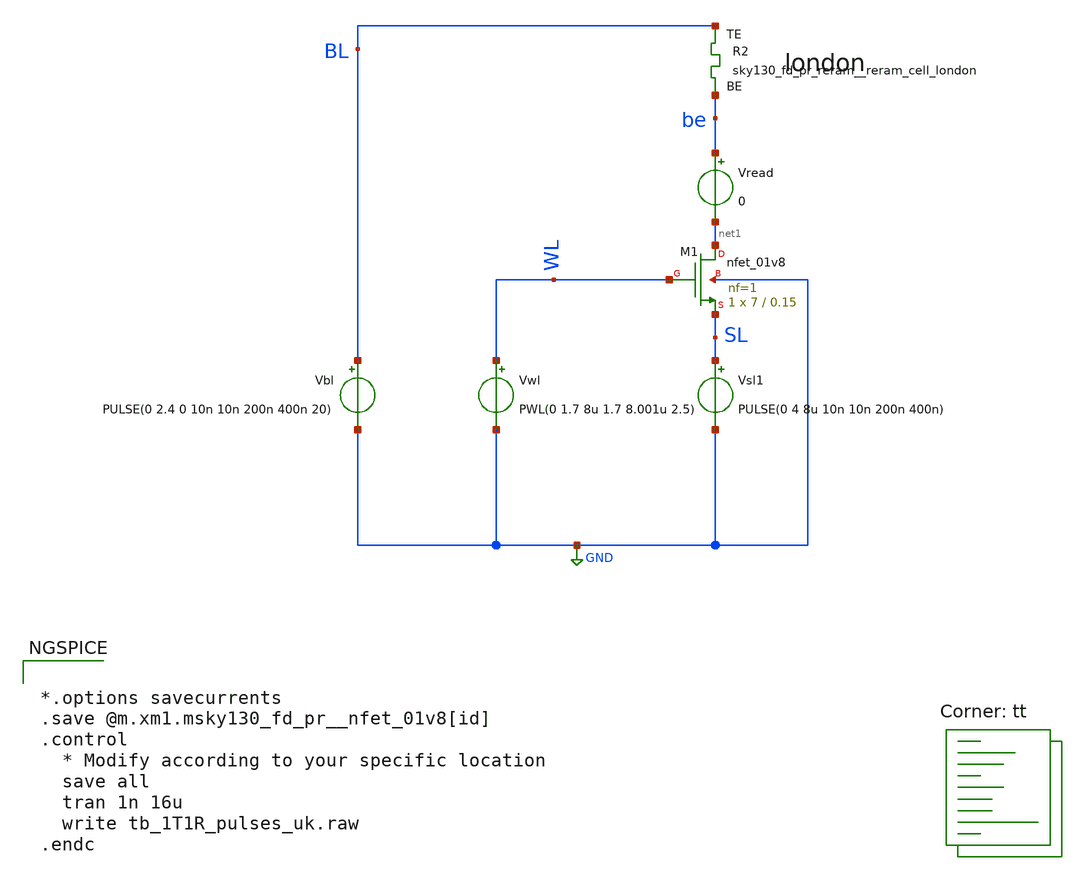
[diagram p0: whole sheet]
** sch_path: memristor_models/rram_london/tb_1T1R_pulses_uk.sch
**.subckt tb_1T1R_pulses_uk
XM1 net1 WL SL GND sky130_fd_pr__nfet_01v8 L=0.15 W=7 nf=1 ad='int((nf+1)/2) * W/nf * 0.29' as='int((nf+2)/2) * W/nf * 0.29'
+ pd='2*int((nf+1)/2) * (W/nf + 0.29)' ps='2*int((nf+2)/2) * (W/nf + 0.29)' nrd='0.29 / W' nrs='0.29 / W'
+ sa=0 sb=0 sd=0 mult=1 m=1
Vwl WL GND PWL(0 1.7 8u 1.7 8.001u 2.5)
Vbl BL GND PULSE(0 2.4 0 10n 10n 200n 400n 20)
XR2 BL be sky130_fd_pr_reram__reram_cell_london
Vread be net1 0
Vsl1 SL GND PULSE(0 4 8u 10n 10n 200n 400n)
**** begin user architecture code


*.options savecurrents
.save @m.xm1.msky130_fd_pr__nfet_01v8[id]
.control
  * Modify according to your specific location
  save all
  tran 1n 16u
  write tb_1T1R_pulses_uk.raw
.endc



.lib $::SKYWATER_MODELS/sky130.lib.spice tt

** opencircuitdesign pdks install
.inc $::SKYWATER_MODELS/sky130_fd_pr_reram__reram_cell_london.spice

**** end user architecture code
**.ends
.GLOBAL GND
.end
